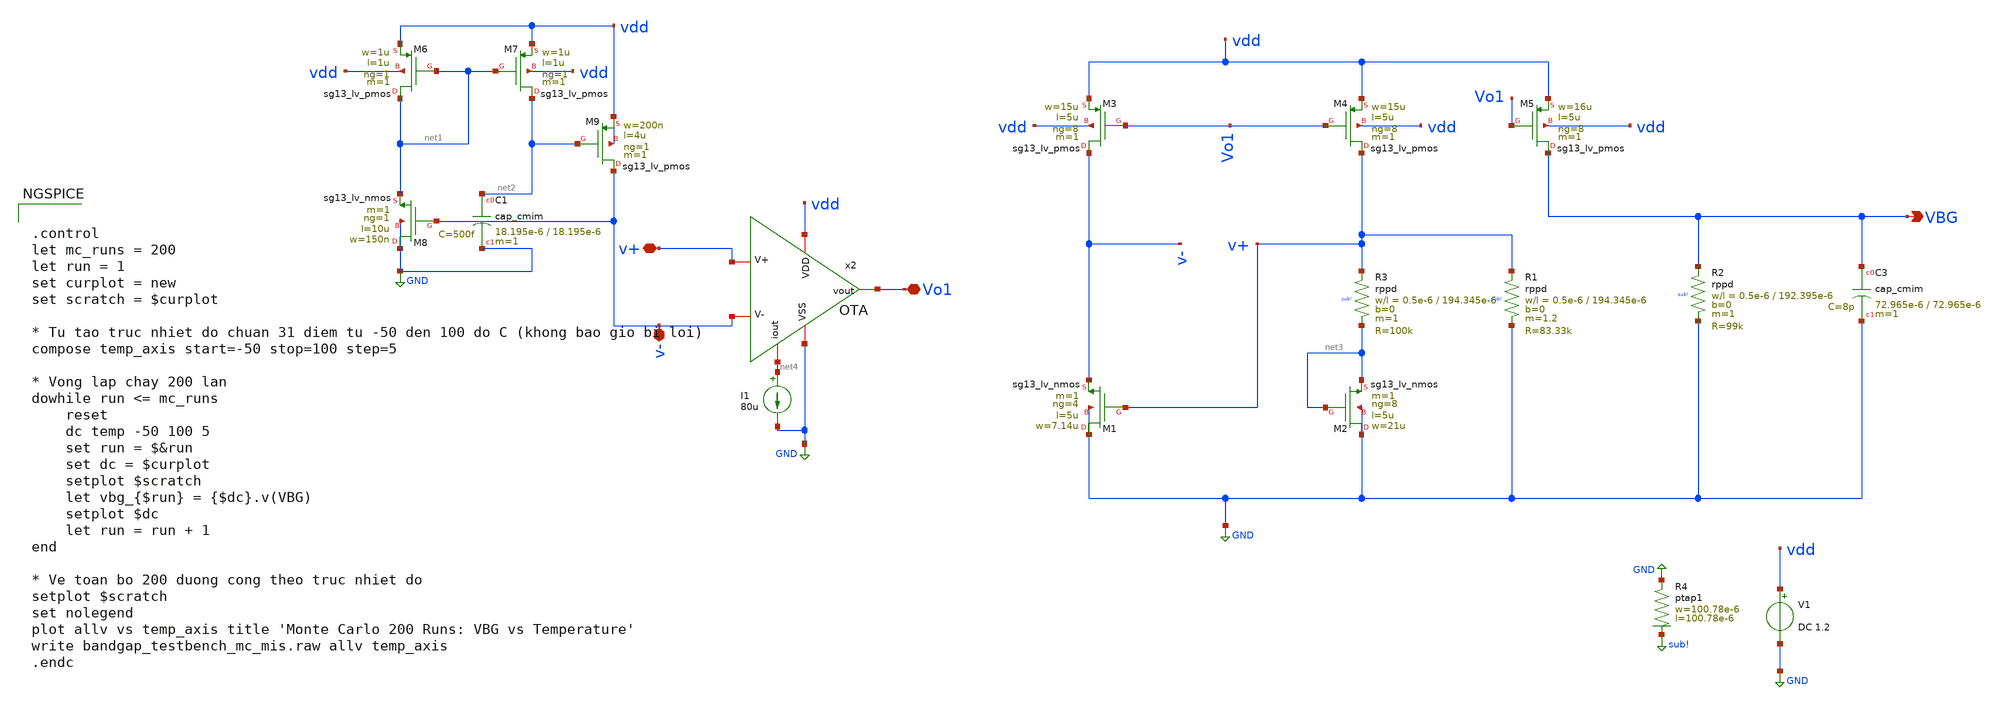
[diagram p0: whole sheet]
** sch_path: BTDay7-Ex/bandgap_MC.sch
**.subckt bandgap_MC v+ v- Vo1 VBG
*.iopin v+
*.iopin v-
*.iopin Vo1
*.opin VBG
XM8 GND v- net1 GND sg13_lv_nmos w=150n l=10u ng=1 m=1 mm_ok=1
XM6 net1 net1 vdd vdd sg13_lv_pmos w=1u l=1u ng=1 m=1 mm_ok=1
XM7 net2 net1 vdd vdd sg13_lv_pmos w=1u l=1u ng=1 m=1 mm_ok=1
XM9 v- net2 vdd vdd sg13_lv_pmos w=200n l=4u ng=1 m=1 mm_ok=1
I1 net4 GND 80u
V1 vdd GND DC 1.2
XM1 GND v+ v- GND sg13_lv_nmos w=7.14u l=5u ng=4 m=1 mm_ok=1
XM2 GND net3 net3 GND sg13_lv_nmos w=21u l=5u ng=8 m=1 mm_ok=1
XM3 v- Vo1 vdd vdd sg13_lv_pmos w=15u l=5u ng=8 m=1 mm_ok=1
XM4 v+ Vo1 vdd vdd sg13_lv_pmos w=15u l=5u ng=8 m=1 mm_ok=1
XM5 VBG Vo1 vdd vdd sg13_lv_pmos w=16u l=5u ng=8 m=1 mm_ok=1
XC3 VBG GND cap_cmim w=72.965e-6 l=72.965e-6 m=1 mm_ok=1
XR3 v+ net3 sub! rppd w=0.5e-6 l=194.345e-6 m=1 b=0 mm_ok=1
XR1 v+ GND sub! rppd w=0.5e-6 l=194.345e-6 m=1.2 b=0 mm_ok=1
XR2 VBG GND sub! rppd w=0.5e-6 l=192.395e-6 m=1 b=0 mm_ok=1
XC1 net2 GND cap_cmim w=18.195e-6 l=18.195e-6 m=1 mm_ok=1
XR4 GND sub! ptap1 R=92.81m w=100.78e-6 l=100.78e-6
x2 v- v+ GND vdd net4 Vo1 OTA
**** begin user architecture code


.control
let mc_runs = 200
let run = 1
set curplot = new
set scratch = $curplot

* Tu tao truc nhiet do chuan 31 diem tu -50 den 100 do C (khong bao gio bi loi)
compose temp_axis start=-50 stop=100 step=5

* Vong lap chay 200 lan
dowhile run <= mc_runs
    reset
    dc temp -50 100 5
    set run = $&run
    set dc = $curplot
    setplot $scratch
    let vbg_{$run} = {$dc}.v(VBG)
    setplot $dc
    let run = run + 1
end

* Ve toan bo 200 duong cong theo truc nhiet do
setplot $scratch
set nolegend
plot allv vs temp_axis title 'Monte Carlo 200 Runs: VBG vs Temperature'
write bandgap_testbench_mc_mis.raw allv temp_axis
.endc



.lib /foss/pdks/ihp-sg13g2/libs.tech/ngspice/models/cornerCAP.lib cap_typ
.lib /foss/pdks/ihp-sg13g2/libs.tech/ngspice/models/cornerRES.lib res_typ
.lib cornerMOSlv.lib mos_tt_mismatch

**** end user architecture code
**.ends

* expanding   symbol:  /foss/designs/BTDay7-Ex/OTA.sym # of pins=6
** sym_path: BTDay7-Ex/OTA.sym
** sch_path: BTDay7-Ex/OTA.sch
.subckt OTA V- V+ VSS VDD iout vout
*.iopin VDD
*.iopin iout
*.iopin V-
*.iopin VSS
*.iopin V+
*.iopin vout
XM6 iout iout VDD VDD sg13_lv_pmos w=75u l=2.08u ng=8 m=1 mm_ok=1
XM7 net1 iout VDD VDD sg13_lv_pmos w=5.3u l=1.95u ng=1 m=1 mm_ok=1
XM8 net3 V- net1 VDD sg13_lv_pmos w=7.41u l=3.64u ng=1 m=1 mm_ok=1
XM9 net2 V+ net1 VDD sg13_lv_pmos w=7.41u l=3.64u ng=1 m=1 mm_ok=1
XM10 net3 net3 VSS VSS sg13_lv_nmos w=720n l=9.75u ng=1 m=1 mm_ok=1
XM11 net2 net3 VSS VSS sg13_lv_nmos w=720n l=9.75u ng=1 m=1 mm_ok=1
XM1 vout net2 VSS VSS sg13_lv_nmos w=28.8u l=9.75u ng=4 m=1 mm_ok=1
XM2 vout iout VDD VDD sg13_lv_pmos w=75u l=2.08u ng=8 m=1 mm_ok=1
XC1 net2 vout cap_cmim w=22.295e-6 l=22.295e-6 m=1 mm_ok=1
.ends

.GLOBAL GND
.GLOBAL sub!
.end
